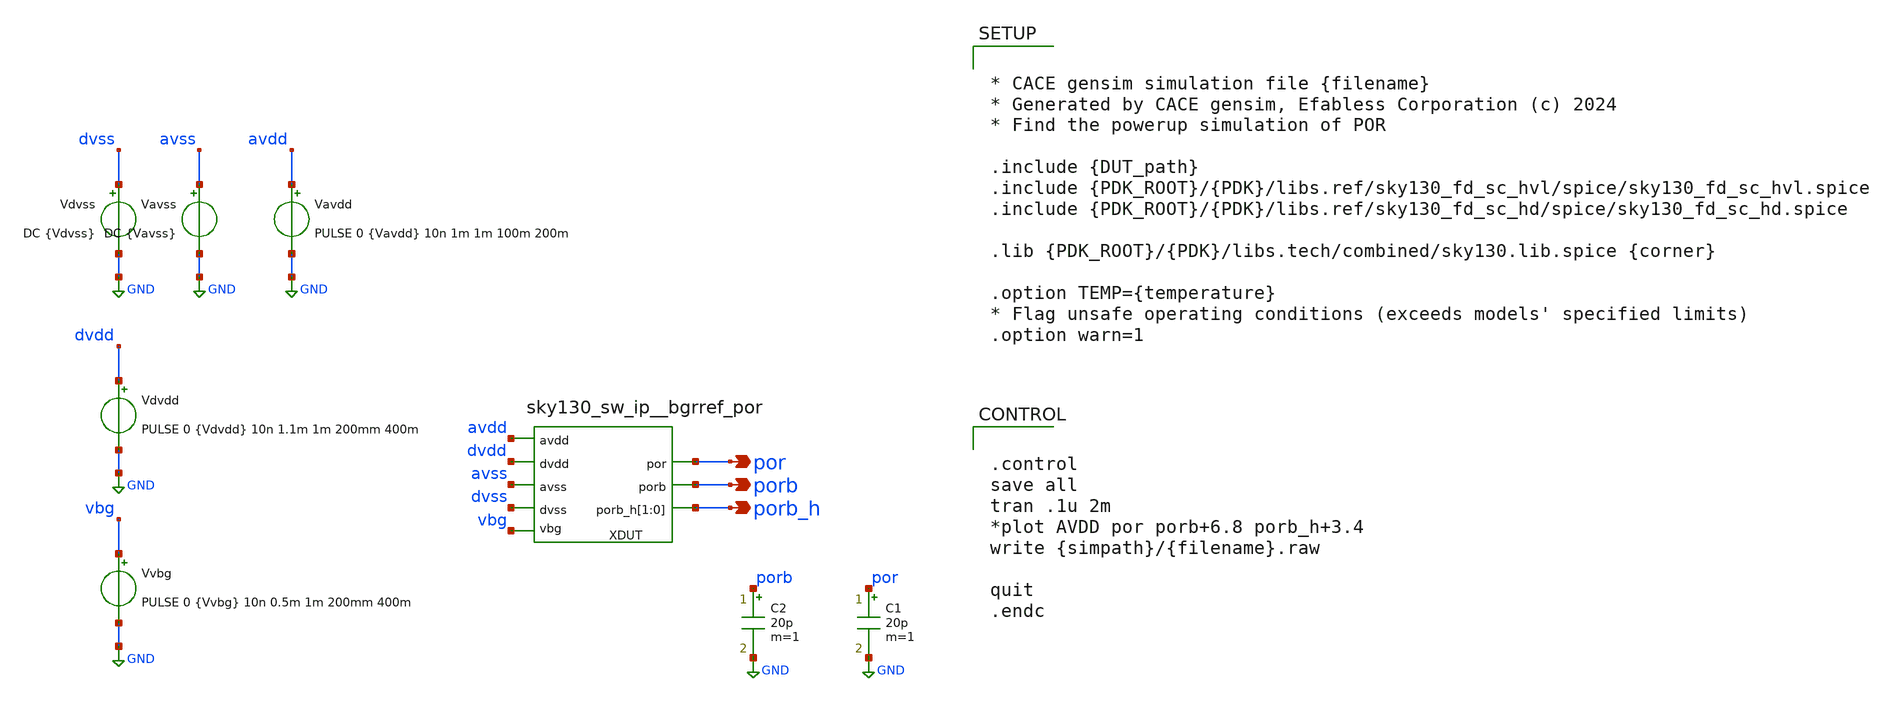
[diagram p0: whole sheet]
** sch_path: xschem/sky130_sw_ip__bgrref_por_tb1.sch
**.subckt sky130_sw_ip__bgrref_por_tb1 por porb porb_h
*.opin por
*.opin porb
*.opin porb_h
Vdvss dvss GND DC {Vdvss}
Vavdd avdd GND PULSE 0 {Vavdd} 10n 1m 1m 100m 200m
Vavss avss GND DC {Vavss}
Vdvdd dvdd GND PULSE 0 {Vdvdd} 10n 1.1m 1m 200mm 400m
Vvbg vbg GND PULSE 0 {Vvbg} 10n 0.5m 1m 200mm 400m
XDUT vbg por avss avdd dvdd porb dvss porb_h porb_h sky130_sw_ip__bgrref_por
C1 por GND 20p m=1
C2 porb GND 20p m=1
**** begin user architecture code


* CACE gensim simulation file {filename}
* Generated by CACE gensim, Efabless Corporation (c) 2024
* Find the powerup simulation of POR

.include {DUT_path}
.include {PDK_ROOT}/{PDK}/libs.ref/sky130_fd_sc_hvl/spice/sky130_fd_sc_hvl.spice
.include {PDK_ROOT}/{PDK}/libs.ref/sky130_fd_sc_hd/spice/sky130_fd_sc_hd.spice

.lib {PDK_ROOT}/{PDK}/libs.tech/combined/sky130.lib.spice {corner}

.option TEMP={temperature}
* Flag unsafe operating conditions (exceeds models' specified limits)
.option warn=1




.control
save all
tran .1u 2m
*plot AVDD por porb+6.8 porb_h+3.4
write {simpath}/{filename}.raw

quit
.endc


**** end user architecture code
**.ends
.GLOBAL GND
.end
